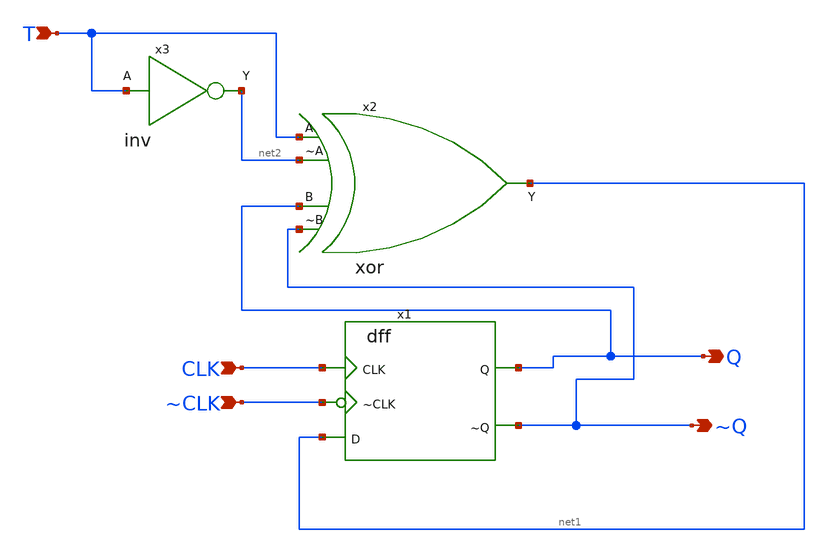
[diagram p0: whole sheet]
** sch_path: circuits/xschem/tff.sch
**.subckt tff T CLK ~CLK Q ~Q
*.ipin T
*.ipin CLK
*.ipin ~CLK
*.opin Q
*.opin ~Q
x1 ~CLK net1 ~Q Q CLK dff
x2 Q net1 T net2 ~Q xor
x3 net2 T inv
**.ends
.end
